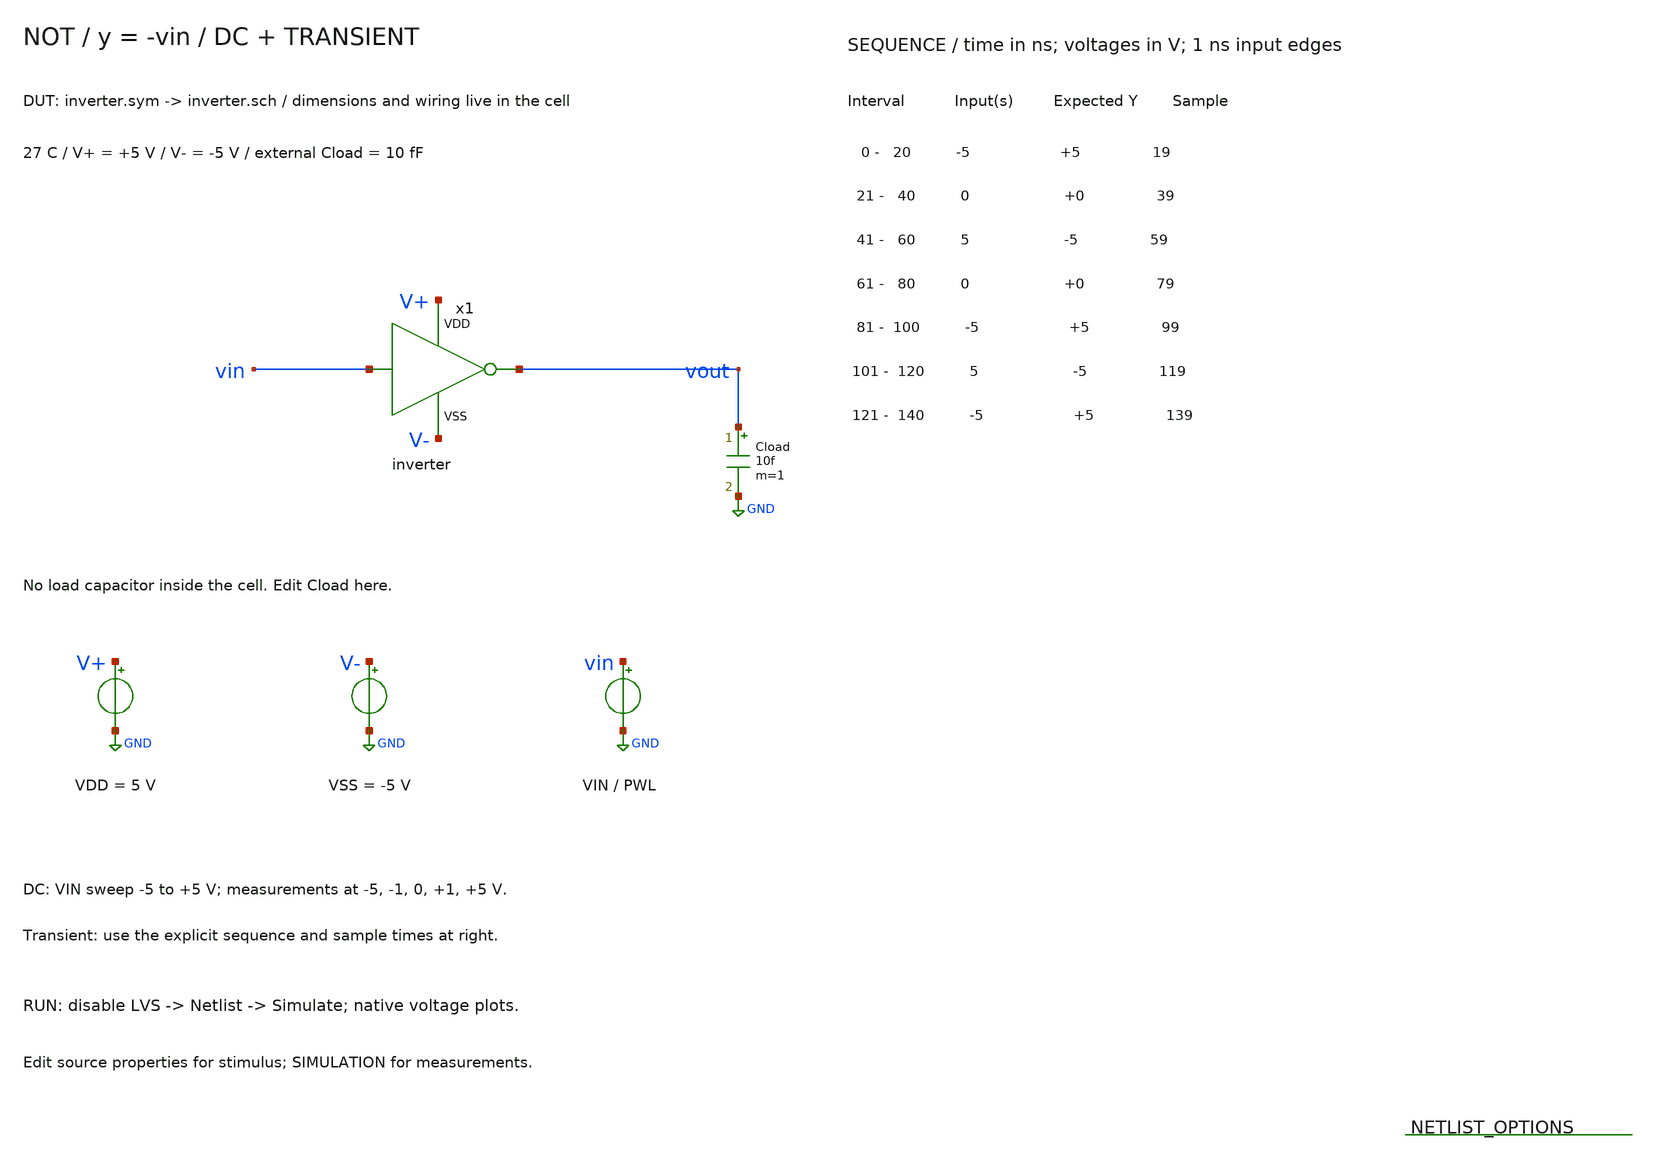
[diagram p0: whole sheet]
** sch_path: member_project/balanced-ternary-logic/PenguinEino/inverter_tb.sch
**.subckt inverter_tb
x1 vin vout V+ V- inverter
Cload vout GND 10f m=1
VDD V+ GND 5
VSS V- GND -5
VIN vin GND PWL(0 -5 20n -5 21n 0 40n 0 41n 5 60n 5 61n 0 80n 0 81n -5 100n -5 101n 5 120n 5 121n -5
+ 140n -5)
**** begin user architecture code
 .include $::LIB/ip62_models

.temp 27
.nodeset v(vout)=5 v(x1.net1)=5 v(x1.net2)=-5
.options rshunt=1e12
.control
save all
dc VIN -5 5 0.015625
meas dc OUT_NEG find v(vout) at=-5
meas dc OUT_ZERO find v(vout) at=0
meas dc OUT_POS find v(vout) at=5
meas dc OUT_MID_LOW find v(vout) at=-1
meas dc OUT_MID_HIGH find v(vout) at=1
plot v(vin) v(vout) ylimit -5.5 5.5 title 'DC transfer: input and output'
reset
tran 0.05n 140n
meas tran OUT_NEG_1 find v(vout) at=19n
meas tran OUT_ZERO_UP find v(vout) at=39n
meas tran OUT_POS_1 find v(vout) at=59n
meas tran OUT_ZERO_DOWN find v(vout) at=79n
meas tran OUT_NEG_2 find v(vout) at=99n
meas tran OUT_POS_2 find v(vout) at=119n
meas tran OUT_NEG_3 find v(vout) at=139n
plot v(vin) v(vout) ylimit -5.5 5.5 title 'Ternary inverter: input and output'
.endc

**** end user architecture code
**.ends

* expanding   symbol:  /home/ishi-kai/balanced-ternary-logic/inverter.sym # of pins=4
** sym_path: member_project/balanced-ternary-logic/PenguinEino/inverter.sym
** sch_path: member_project/balanced-ternary-logic/PenguinEino/inverter.sch
.subckt inverter vin vout VDD VSS
*.iopin VDD
*.ipin vin
*.opin vout
*.iopin VSS
XXM1 net1 vin VDD VDD PMOS w=13.5u l=1u nrd=0 nrs=0 m=1
XR1 net1 vout VDD F_RR w=2.8e-06 l=30e-06 R=1 tc1=0 tc2=0 m=1
XR2 vout net2 VDD F_RR w=2.8e-06 l=30e-06 R=1 tc1=0 tc2=0 m=1
XXM2 net2 vin VSS VSS NMOS w=5u l=1u nrd=0 nrs=0 m=1
.ends

.GLOBAL GND
.end
